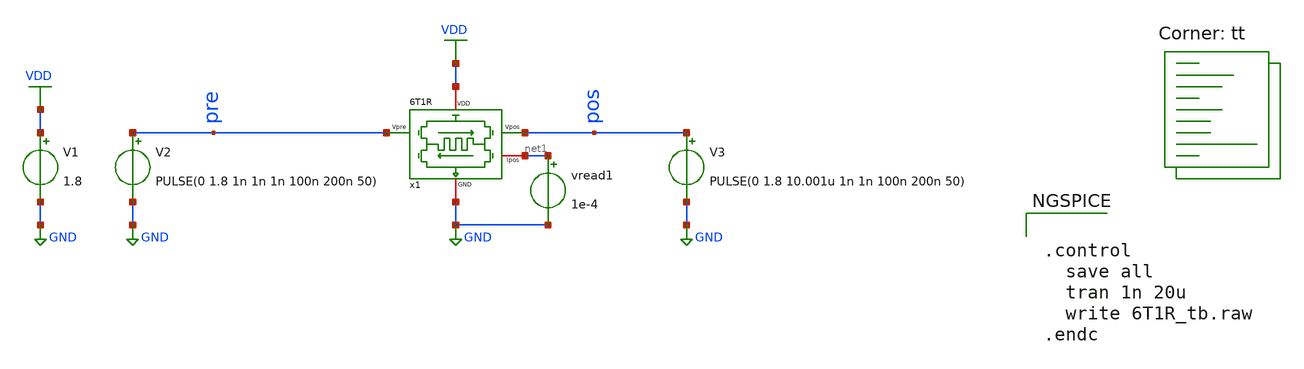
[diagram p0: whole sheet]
** sch_path: synapse/6T1R_tb.sch
**.subckt 6T1R_tb
V2 pre GND PULSE(0 1.8 1n 1n 1n 100n 200n 50)
V1 VDD GND 1.8
V3 pos GND PULSE(0 1.8 10.001u 1n 1n 100n 200n 50)
vread1 net1 GND 1e-4
x1 VDD net1 pre pos GND 6T1R
**** begin user architecture code
.lib $::SKYWATER_MODELS/sky130.lib.spice tt

** opencircuitdesign pdks install
.inc $::SKYWATER_MODELS/rram_v0.spice



.control
  save all
  tran 1n 20u
  write 6T1R_tb.raw
.endc


**** end user architecture code
**.ends

* expanding   symbol:  /home/ricardo/RATT_repos/Proyectos_xschem/synapse/6T1R.sym # of pins=5
** sym_path: synapse/6T1R.sym
** sch_path: synapse/6T1R.sch
.subckt 6T1R VDD Ipos Vpre Vpos GND
*.ipin Vpre
*.ipin Vpos
*.iopin GND
*.iopin Ipos
*.iopin VDD
XM1 vipre Vpre net1 GND sky130_fd_pr__nfet_01v8 L=0.15 W=10 nf=1 ad='int((nf+1)/2) * W/nf * 0.29' as='int((nf+2)/2) * W/nf * 0.29'
+ pd='2*int((nf+1)/2) * (W/nf + 0.29)' ps='2*int((nf+2)/2) * (W/nf + 0.29)' nrd='0.29 / W' nrs='0.29 / W'
+ sa=0 sb=0 sd=0 mult=1 m=1
XR1 net2 net1 rram_v0
XM3 vipre Vpos net2 GND sky130_fd_pr__nfet_01v8 L=0.15 W=1 nf=1 ad='int((nf+1)/2) * W/nf * 0.29' as='int((nf+2)/2) * W/nf * 0.29'
+ pd='2*int((nf+1)/2) * (W/nf + 0.29)' ps='2*int((nf+2)/2) * (W/nf + 0.29)' nrd='0.29 / W' nrs='0.29 / W'
+ sa=0 sb=0 sd=0 mult=1 m=1
XM6 Ipos vipre VDD VDD sky130_fd_pr__pfet_01v8 L=0.15 W=1 nf=1 ad='int((nf+1)/2) * W/nf * 0.29' as='int((nf+2)/2) * W/nf * 0.29'
+ pd='2*int((nf+1)/2) * (W/nf + 0.29)' ps='2*int((nf+2)/2) * (W/nf + 0.29)' nrd='0.29 / W' nrs='0.29 / W'
+ sa=0 sb=0 sd=0 mult=1 m=1
XM5 vipre vipre VDD VDD sky130_fd_pr__pfet_01v8 L=0.15 W=20 nf=1 ad='int((nf+1)/2) * W/nf * 0.29' as='int((nf+2)/2) * W/nf * 0.29'
+ pd='2*int((nf+1)/2) * (W/nf + 0.29)' ps='2*int((nf+2)/2) * (W/nf + 0.29)' nrd='0.29 / W' nrs='0.29 / W'
+ sa=0 sb=0 sd=0 mult=1 m=1
XM2 net1 Vpos GND GND sky130_fd_pr__nfet_01v8 L=0.15 W=1 nf=1 ad='int((nf+1)/2) * W/nf * 0.29' as='int((nf+2)/2) * W/nf * 0.29'
+ pd='2*int((nf+1)/2) * (W/nf + 0.29)' ps='2*int((nf+2)/2) * (W/nf + 0.29)' nrd='0.29 / W' nrs='0.29 / W'
+ sa=0 sb=0 sd=0 mult=1 m=1
XM4 net2 Vpre GND GND sky130_fd_pr__nfet_01v8 L=0.15 W=10 nf=1 ad='int((nf+1)/2) * W/nf * 0.29' as='int((nf+2)/2) * W/nf * 0.29'
+ pd='2*int((nf+1)/2) * (W/nf + 0.29)' ps='2*int((nf+2)/2) * (W/nf + 0.29)' nrd='0.29 / W' nrs='0.29 / W'
+ sa=0 sb=0 sd=0 mult=1 m=1
.ends

.GLOBAL GND
.GLOBAL VDD
.end
